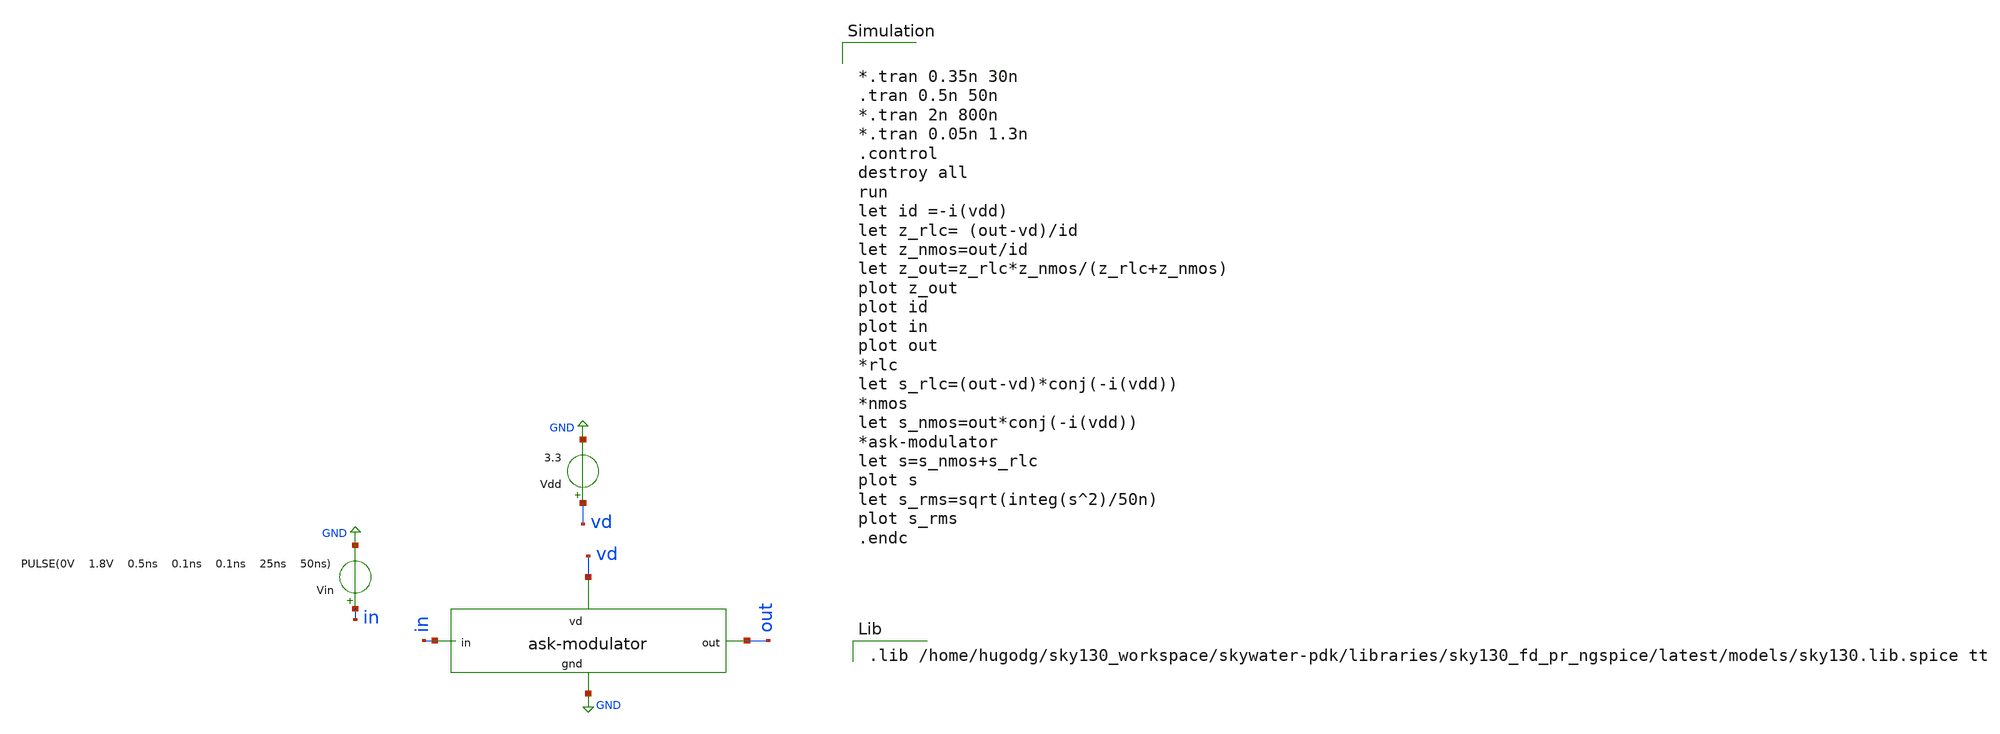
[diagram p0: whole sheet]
** sch_path: ask_modulator/xschem/ask-modulator_tb-tran.sch
**.subckt ask-modulator_tb-tran
Vdd vd GND 3.3
Vin in GND PULSE(0V 1.8V 0.5ns 0.1ns 0.1ns 25ns 50ns)
x1 vd out in GND ask-modulator
**** begin user architecture code


*.tran 0.35n 30n
.tran 0.5n 50n
*.tran 2n 800n
*.tran 0.05n 1.3n
.control
destroy all
run
let id =-i(vdd)
let z_rlc= (out-vd)/id
let z_nmos=out/id
let z_out=z_rlc*z_nmos/(z_rlc+z_nmos)
plot z_out
plot id
plot in
plot out
*rlc
let s_rlc=(out-vd)*conj(-i(vdd))
*nmos
let s_nmos=out*conj(-i(vdd))
*ask-modulator
let s=s_nmos+s_rlc
plot s
let s_rms=sqrt(integ(s^2)/50n)
plot s_rms
.endc


.lib /home/hugodg/sky130_workspace/skywater-pdk/libraries/sky130_fd_pr_ngspice/latest/models/sky130.lib.spice tt

**** end user architecture code
**.ends
.GLOBAL GND
.end
